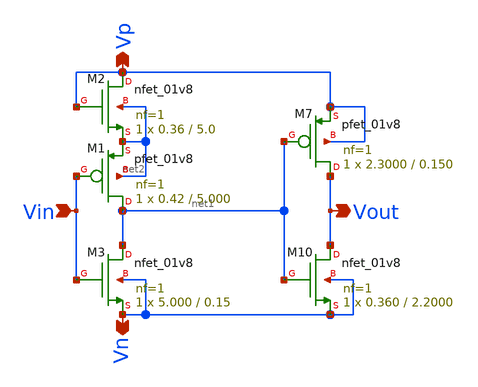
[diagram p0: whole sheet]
** sch_path: xschem/Vth_sch/Symbol/th03.sch
**.subckt th03 Vn Vp Vin Vout
*.opin Vn
*.opin Vp
*.ipin Vin
*.opin Vout
XM7 Vout net1 Vp Vp sky130_fd_pr__pfet_01v8 L=0.150 W=2.3000 nf=1 ad='int((nf+1)/2) * W/nf * 0.29' as='int((nf+2)/2) * W/nf * 0.29'
+ pd='2*int((nf+1)/2) * (W/nf + 0.29)' ps='2*int((nf+2)/2) * (W/nf + 0.29)' nrd='0.29 / W' nrs='0.29 / W'
+ sa=0 sb=0 sd=0 mult=1 m=1
XM10 Vout net1 Vn Vn sky130_fd_pr__nfet_01v8 L=2.2000 W=0.360 nf=1 ad='int((nf+1)/2) * W/nf * 0.29' as='int((nf+2)/2) * W/nf * 0.29'
+ pd='2*int((nf+1)/2) * (W/nf + 0.29)' ps='2*int((nf+2)/2) * (W/nf + 0.29)' nrd='0.29 / W' nrs='0.29 / W'
+ sa=0 sb=0 sd=0 mult=1 m=1
XM1 net1 Vin net2 net2 sky130_fd_pr__pfet_01v8 L=5.000 W=0.42 nf=1 ad='int((nf+1)/2) * W/nf * 0.29' as='int((nf+2)/2) * W/nf * 0.29'
+ pd='2*int((nf+1)/2) * (W/nf + 0.29)' ps='2*int((nf+2)/2) * (W/nf + 0.29)' nrd='0.29 / W' nrs='0.29 / W'
+ sa=0 sb=0 sd=0 mult=1 m=1
XM3 net1 Vin Vn Vn sky130_fd_pr__nfet_01v8 L=0.15 W=5.000 nf=1 ad='int((nf+1)/2) * W/nf * 0.29' as='int((nf+2)/2) * W/nf * 0.29'
+ pd='2*int((nf+1)/2) * (W/nf + 0.29)' ps='2*int((nf+2)/2) * (W/nf + 0.29)' nrd='0.29 / W' nrs='0.29 / W'
+ sa=0 sb=0 sd=0 mult=1 m=1
XM2 Vp Vp net2 net2 sky130_fd_pr__nfet_01v8 L=5.0 W=0.36 nf=1 ad='int((nf+1)/2) * W/nf * 0.29' as='int((nf+2)/2) * W/nf * 0.29'
+ pd='2*int((nf+1)/2) * (W/nf + 0.29)' ps='2*int((nf+2)/2) * (W/nf + 0.29)' nrd='0.29 / W' nrs='0.29 / W'
+ sa=0 sb=0 sd=0 mult=1 m=1
**.ends
.end
